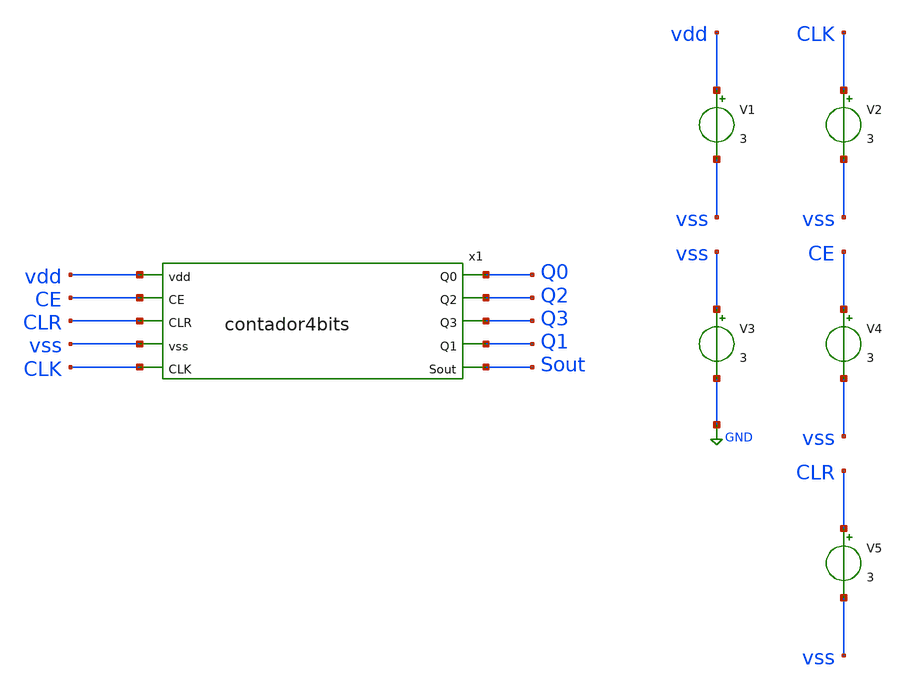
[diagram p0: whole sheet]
** sch_path: track_vlsi/lapi-fernandez/sch/tb_contador4bits_bis.sch
**.subckt tb_contador4bits_bis
x1 vdd Q0 Q2 Q3 Q1 CE CLR Sout vss CLK contador4bits
V1 vdd vss 3
V2 CLK vss 3
V3 vss GND 3
V4 CE vss 3
V5 CLR vss 3
**** begin user architecture code



*Circuits Params

.param Vin = 1.8
*.param vin2 = 1.8
.options TEMP = 27.0

*include

.lib /home/eamta/skywater/skywater-pdk/libraries/sky130_fd_pr_ngspice/latest/models/corners/sky130.lib TT

*signals to SAVE

.save all
*+ @M.x1.xm1.msky130_fd_pr__nfet_01v8[id]  @M.x1.xm1.msky130_fd_pr__nfet_01v8[gm]
*+ @M.x1.xm2.msky130_fd_pr__nfet_01v8[id]  @M.x1.xm2.msky130_fd_pr__nfet_01v8[gm]
*+ @M.x1.xm3.msky130_fd_pr__nfet_01v8[id]  @M.x1.xm3.msky130_fd_pr__nfet_01v8[gm]
*+ @M.x1.xm4.msky130_fd_pr__pfet_01v8[id]  @M.x1.xm4.msky130_fd_pr__pfet_01v8[gm]
*+ @M.x1.xm5.msky130_fd_pr__pfet_01v8[id]  @M.x1.xm5.msky130_fd_pr__pfet_01v8[gm]
*+ @M.x1.xm6.msky130_fd_pr__pfet_01v8[id]  @M.x1.xm6.msky130_fd_pr__pfet_01v8[gm]


*simulation

.control
  tran 0.1n 1n
  setplot tran1
  plot v(CLK)
  write tb_and_tran.raw


 * reset
 * dc v3 0 1.8 0.01
 * setplot dc1
 * plot v(out) v(vin1) v(vin2)
 * write tb_and_dc.raw

 * reset
 * op

 * set filetype= ASCII

  write tb_and.raw
  print all


.endc

.end





**** end user architecture code
**.ends
.GLOBAL GND
.end
